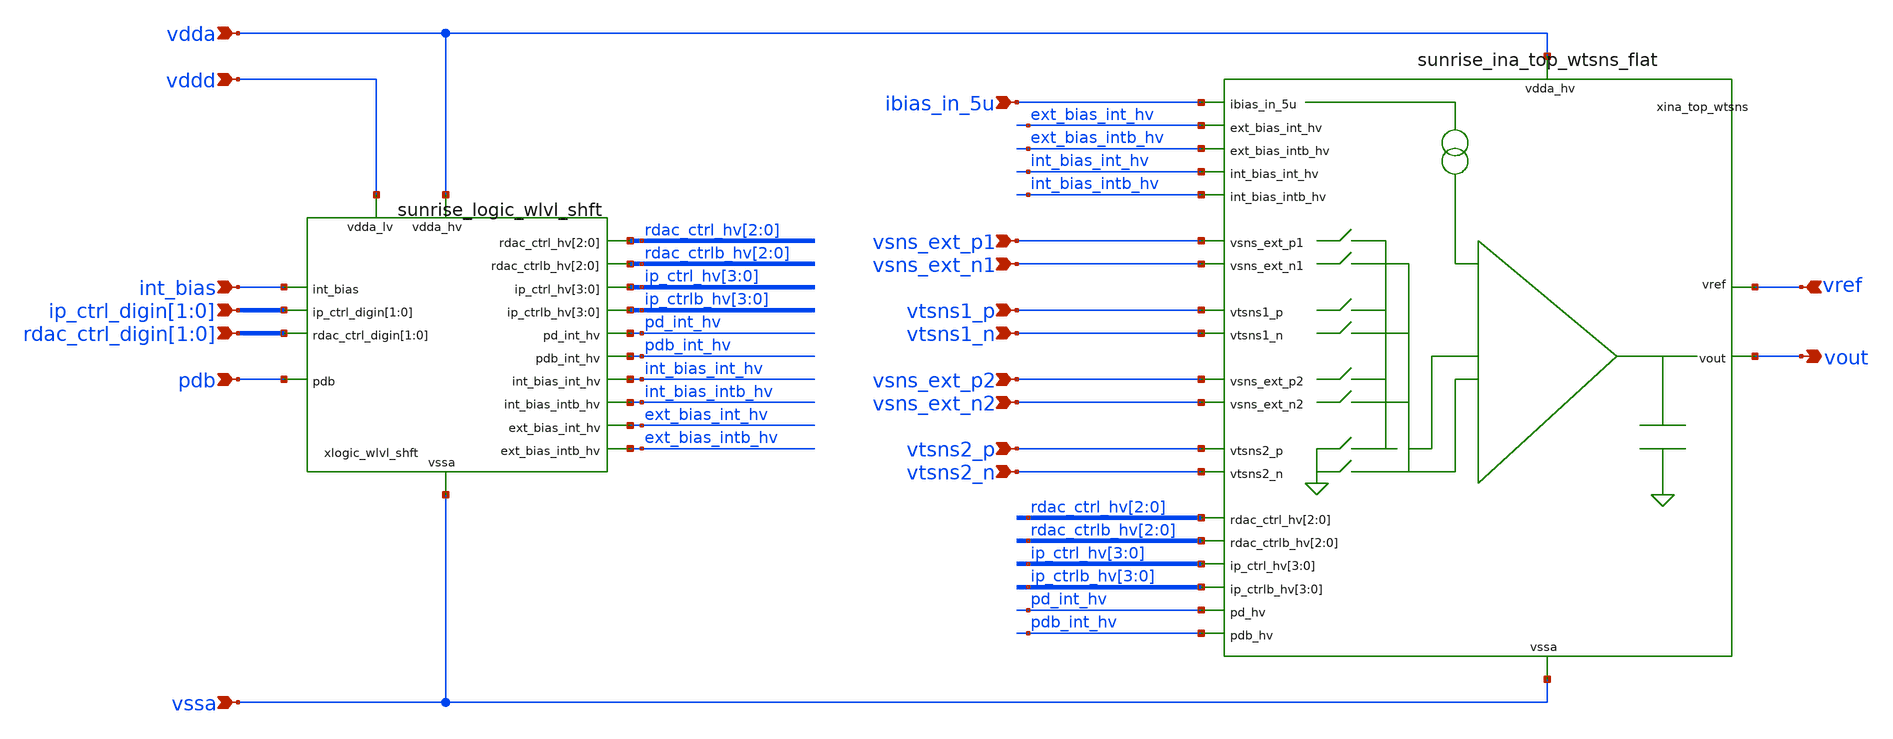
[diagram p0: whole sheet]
** sch_path: Schematics_Layout/sunrise_ina_top_wtsns_logic/sunrise_ina_top_wtsns_logic.sch
**.subckt sunrise_ina_top_wtsns_logic ibias_in_5u vsns_ext_p1 vsns_ext_n1 vsns_ext_p2 vsns_ext_n2
*+ vtsns1_p vtsns1_n vtsns2_p vtsns2_n vdda vssa int_bias ip_ctrl_digin[1],ip_ctrl_digin[0]
*+ rdac_ctrl_digin[1],rdac_ctrl_digin[0] pdb vddd vref vout
*.ipin ibias_in_5u
*.ipin vsns_ext_p1
*.ipin vsns_ext_n1
*.ipin vsns_ext_p2
*.ipin vsns_ext_n2
*.ipin vtsns1_p
*.ipin vtsns1_n
*.ipin vtsns2_p
*.ipin vtsns2_n
*.ipin vdda
*.ipin vssa
*.ipin int_bias
*.ipin ip_ctrl_digin[1],ip_ctrl_digin[0]
*.ipin rdac_ctrl_digin[1],rdac_ctrl_digin[0]
*.ipin pdb
*.ipin vddd
*.ipin vref
*.opin vout
xina_top_wtsns vdda ibias_in_5u ext_bias_int_hv ext_bias_intb_hv int_bias_int_hv vtsns1_n vtsns1_p
+ vtsns2_n vtsns2_p int_bias_intb_hv vsns_ext_p1 vsns_ext_n1 vref vout vsns_ext_p2 vsns_ext_n2 rdac_ctrl_hv[2]
+ rdac_ctrl_hv[1] rdac_ctrl_hv[0] rdac_ctrlb_hv[2] rdac_ctrlb_hv[1] rdac_ctrlb_hv[0] ip_ctrl_hv[3] ip_ctrl_hv[2]
+ ip_ctrl_hv[1] ip_ctrl_hv[0] ip_ctrlb_hv[3] ip_ctrlb_hv[2] ip_ctrlb_hv[1] ip_ctrlb_hv[0] pd_int_hv pdb_int_hv vssa
+ sunrise_ina_top_wtsns_flat
xlogic_wlvl_shft vdda vddd rdac_ctrl_hv[2] rdac_ctrl_hv[1] rdac_ctrl_hv[0] rdac_ctrlb_hv[2]
+ rdac_ctrlb_hv[1] rdac_ctrlb_hv[0] ip_ctrl_hv[3] ip_ctrl_hv[2] ip_ctrl_hv[1] ip_ctrl_hv[0] ip_ctrlb_hv[3]
+ ip_ctrlb_hv[2] ip_ctrlb_hv[1] ip_ctrlb_hv[0] int_bias ip_ctrl_digin[1] ip_ctrl_digin[0] rdac_ctrl_digin[1]
+ rdac_ctrl_digin[0] pdb pdb_int_hv pd_int_hv int_bias_int_hv int_bias_intb_hv ext_bias_int_hv ext_bias_intb_hv vssa
+ sunrise_logic_wlvl_shft
**.ends
.end
